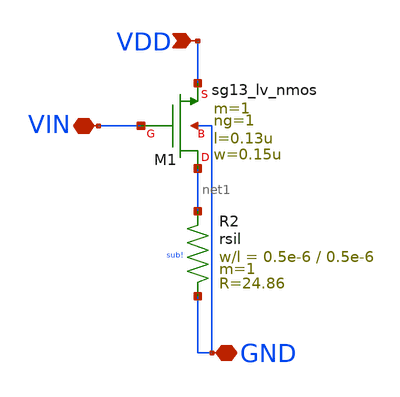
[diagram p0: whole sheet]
** sch_path: developpement/LVS/LAYOUT/test_resistance/test_resistance.sch
**.subckt test_resistance VIN VDD GND
*.iopin VIN
*.ipin VDD
*.iopin GND
XR2 net1 GND sub! rsil w=0.5e-6 l=0.5e-6 m=1 mm_ok=1
XM1 net1 VIN VDD GND sg13_lv_nmos w=0.15u l=0.13u ng=1 m=1 mm_ok=1
**.ends
.end
